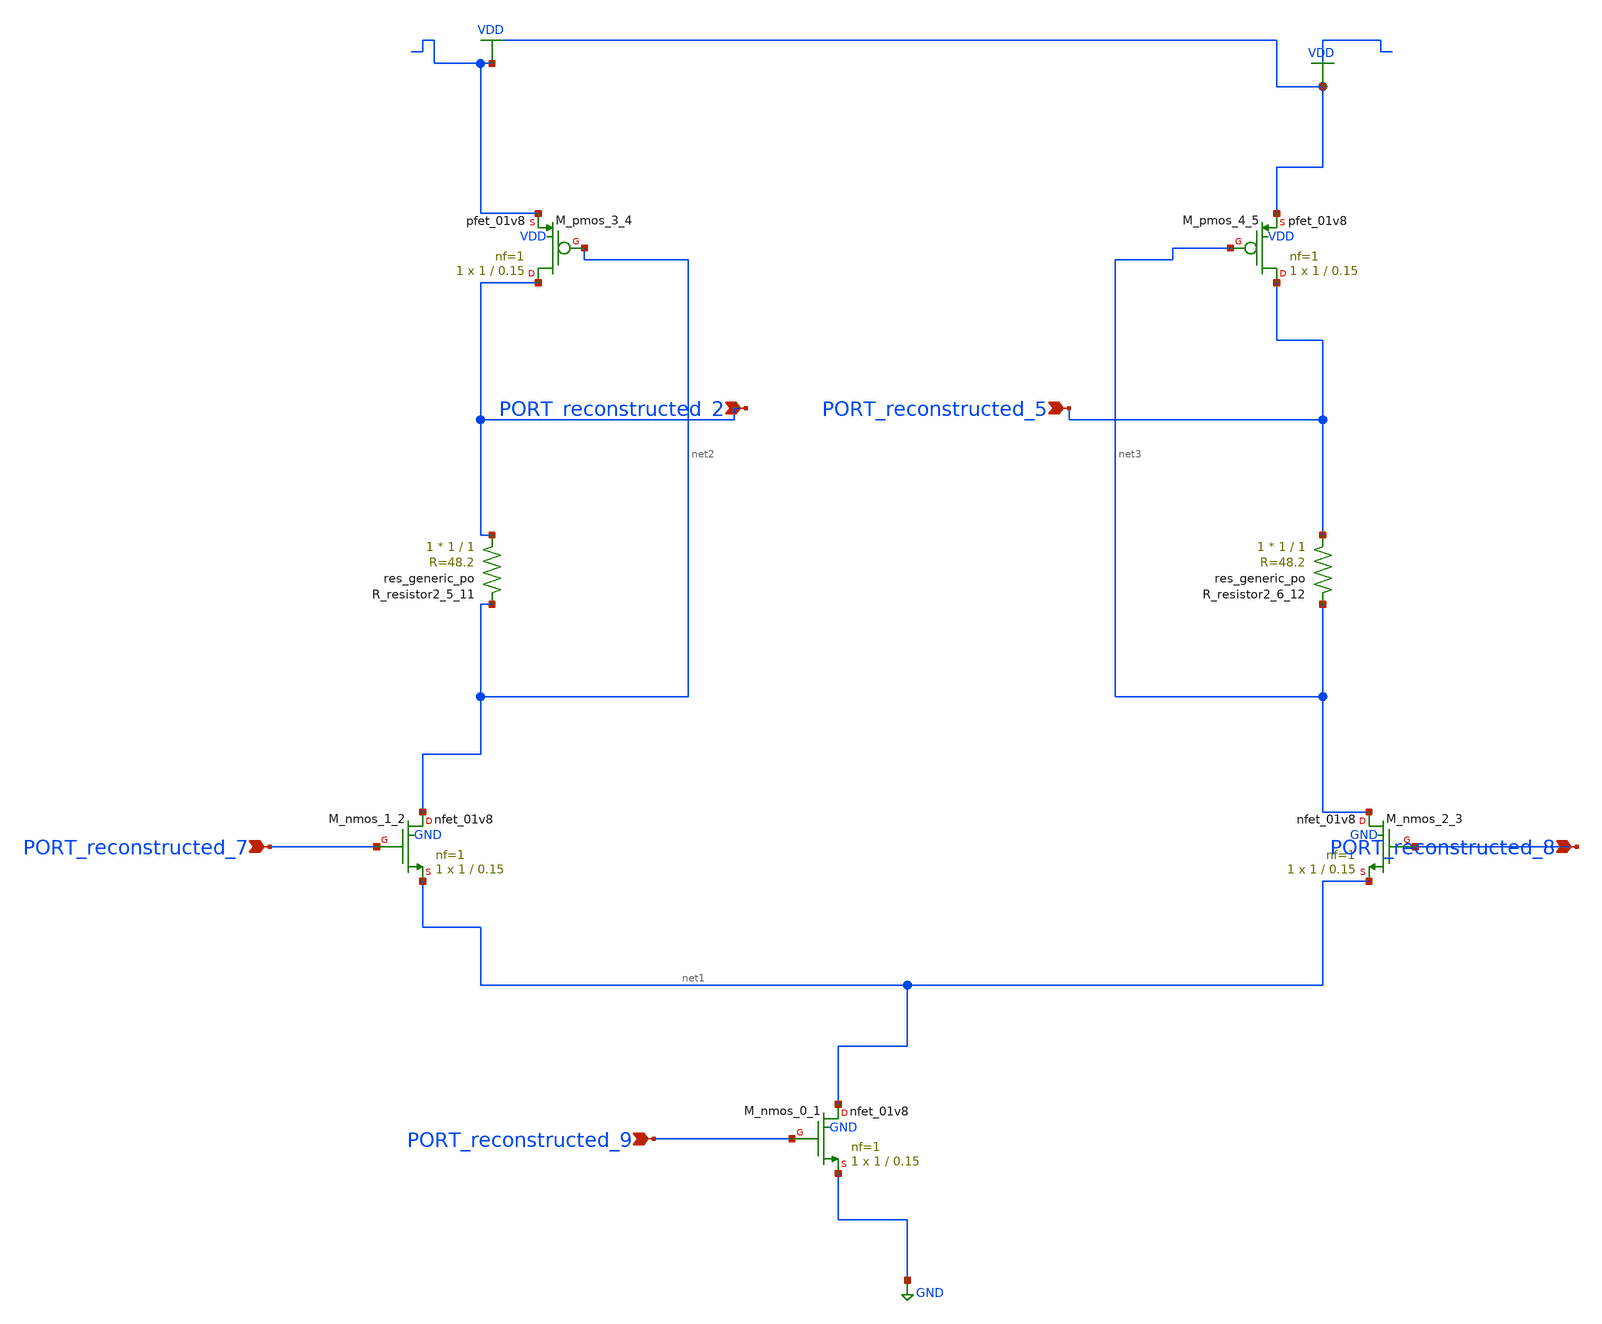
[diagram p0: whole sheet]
** sch_path: schematics/AMSNet/241.sch
**.subckt 241 PORT_reconstructed_2 PORT_reconstructed_7 PORT_reconstructed_8 PORT_reconstructed_5
*+ PORT_reconstructed_9
*.ipin PORT_reconstructed_2
*.ipin PORT_reconstructed_7
*.ipin PORT_reconstructed_8
*.ipin PORT_reconstructed_5
*.ipin PORT_reconstructed_9
XM_nmos_0_1 net1 PORT_reconstructed_9 GND GND sky130_fd_pr__nfet_01v8 L=0.15 W=1 nf=1 ad='int((1 + 1)/2) * 1 / 1 * 0.29'
+ as='int((1 + 2)/2) * 1 / 1 * 0.29' pd='2*int((1 + 1)/2) * (1 / 1 + 0.29)' ps='2*int((1 + 2)/2) * (1 / 1 + 0.29)'
+ nrd='0.29 / 1 ' nrs='0.29 / 1 ' sa=0 sb=0 sd=0 mult=1 m=1
XM_nmos_1_2 net2 PORT_reconstructed_7 net1 GND sky130_fd_pr__nfet_01v8 L=0.15 W=1 nf=1 ad='int((1 + 1)/2) * 1 / 1 * 0.29'
+ as='int((1 + 2)/2) * 1 / 1 * 0.29' pd='2*int((1 + 1)/2) * (1 / 1 + 0.29)' ps='2*int((1 + 2)/2) * (1 / 1 + 0.29)'
+ nrd='0.29 / 1 ' nrs='0.29 / 1 ' sa=0 sb=0 sd=0 mult=1 m=1
XM_nmos_2_3 net3 PORT_reconstructed_8 net1 GND sky130_fd_pr__nfet_01v8 L=0.15 W=1 nf=1 ad='int((1 + 1)/2) * 1 / 1 * 0.29'
+ as='int((1 + 2)/2) * 1 / 1 * 0.29' pd='2*int((1 + 1)/2) * (1 / 1 + 0.29)' ps='2*int((1 + 2)/2) * (1 / 1 + 0.29)'
+ nrd='0.29 / 1 ' nrs='0.29 / 1 ' sa=0 sb=0 sd=0 mult=1 m=1
XM_pmos_3_4 PORT_reconstructed_2 net2 VDD VDD sky130_fd_pr__pfet_01v8 L=0.15 W=1 nf=1 ad='int((1 + 1)/2) * 1 / 1 * 0.29'
+ as='int((1 + 2)/2) * 1 / 1 * 0.29' pd='2*int((1 + 1)/2) * (1 / 1 + 0.29)' ps='2*int((1 + 2)/2) * (1 / 1 + 0.29)'
+ nrd='0.29 / 1 ' nrs='0.29 / 1 ' sa=0 sb=0 sd=0 mult=1 m=1
XM_pmos_4_5 PORT_reconstructed_5 net3 VDD VDD sky130_fd_pr__pfet_01v8 L=0.15 W=1 nf=1 ad='int((1 + 1)/2) * 1 / 1 * 0.29'
+ as='int((1 + 2)/2) * 1 / 1 * 0.29' pd='2*int((1 + 1)/2) * (1 / 1 + 0.29)' ps='2*int((1 + 2)/2) * (1 / 1 + 0.29)'
+ nrd='0.29 / 1 ' nrs='0.29 / 1 ' sa=0 sb=0 sd=0 mult=1 m=1
XR_resistor2_5_11 PORT_reconstructed_2 net2 sky130_fd_pr__res_generic_po W=1 L=1 m=1
XR_resistor2_6_12 PORT_reconstructed_5 net3 sky130_fd_pr__res_generic_po W=1 L=1 m=1
**.ends
.GLOBAL GND
.GLOBAL VDD
.end
